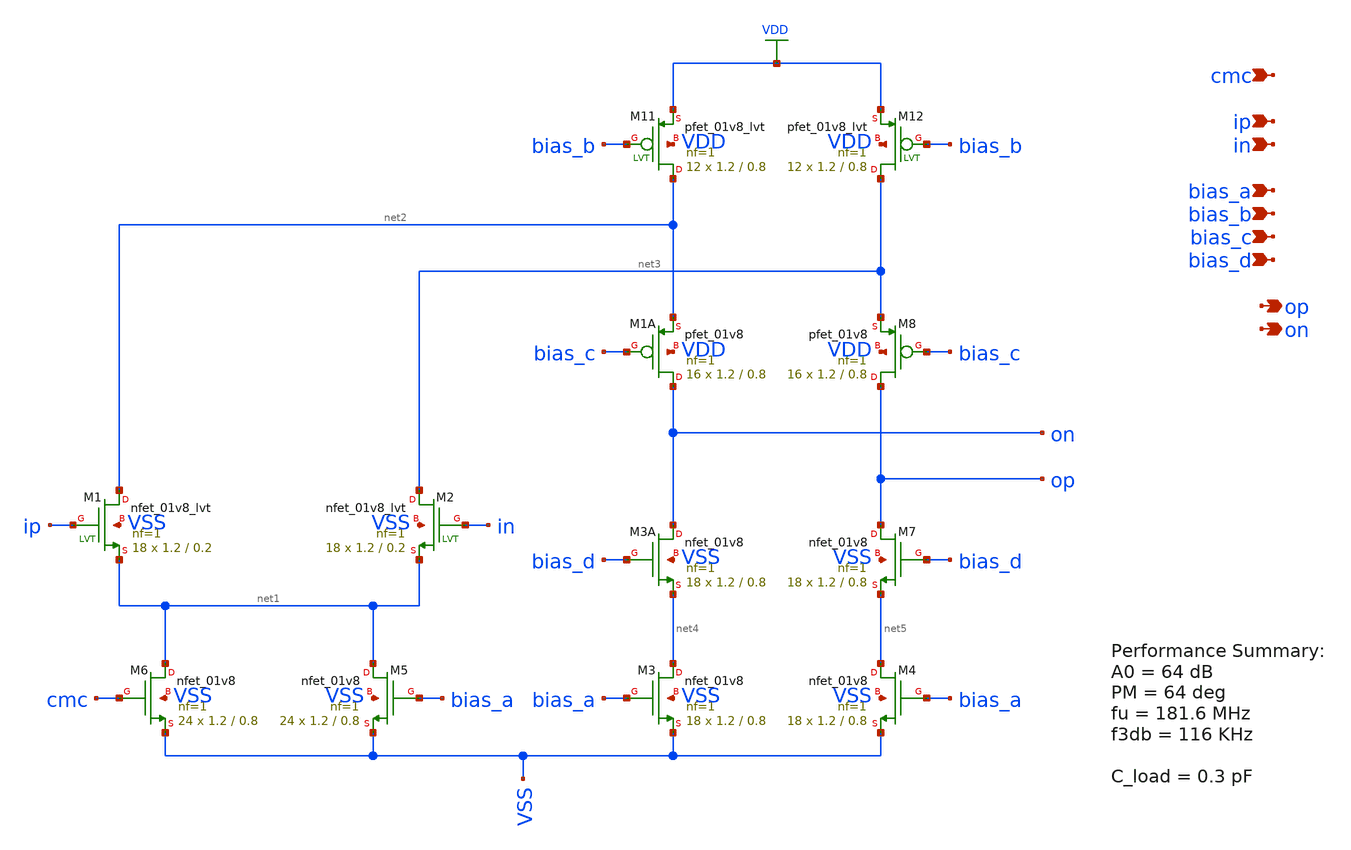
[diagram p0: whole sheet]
** sch_path: design/schematic/folded_cascode_2_core.sch
**.subckt folded_cascode_2_core cmc ip in bias_a bias_b bias_c bias_d op on
*.ipin cmc
*.ipin ip
*.ipin in
*.ipin bias_a
*.ipin bias_b
*.ipin bias_c
*.ipin bias_d
*.opin op
*.opin on
XM1 net2 ip net1 VSS sky130_fd_pr__nfet_01v8_lvt L=0.2 W=1.2 nf=1 ad='int((nf+1)/2) * W/nf * 0.29' as='int((nf+2)/2) * W/nf * 0.29'
+ pd='2*int((nf+1)/2) * (W/nf + 0.29)' ps='2*int((nf+2)/2) * (W/nf + 0.29)' nrd='0.29 / W' nrs='0.29 / W'
+ sa=0 sb=0 sd=0 mult=18 m=18
XM2 net3 in net1 VSS sky130_fd_pr__nfet_01v8_lvt L=0.2 W=1.2 nf=1 ad='int((nf+1)/2) * W/nf * 0.29' as='int((nf+2)/2) * W/nf * 0.29'
+ pd='2*int((nf+1)/2) * (W/nf + 0.29)' ps='2*int((nf+2)/2) * (W/nf + 0.29)' nrd='0.29 / W' nrs='0.29 / W'
+ sa=0 sb=0 sd=0 mult=18 m=18
XM6 net1 cmc VSS VSS sky130_fd_pr__nfet_01v8 L=0.8 W=1.2 nf=1 ad='int((nf+1)/2) * W/nf * 0.29' as='int((nf+2)/2) * W/nf * 0.29'
+ pd='2*int((nf+1)/2) * (W/nf + 0.29)' ps='2*int((nf+2)/2) * (W/nf + 0.29)' nrd='0.29 / W' nrs='0.29 / W'
+ sa=0 sb=0 sd=0 mult=24 m=24
XM5 net1 bias_a VSS VSS sky130_fd_pr__nfet_01v8 L=0.8 W=1.2 nf=1 ad='int((nf+1)/2) * W/nf * 0.29' as='int((nf+2)/2) * W/nf * 0.29'
+ pd='2*int((nf+1)/2) * (W/nf + 0.29)' ps='2*int((nf+2)/2) * (W/nf + 0.29)' nrd='0.29 / W' nrs='0.29 / W'
+ sa=0 sb=0 sd=0 mult=24 m=24
XM11 net2 bias_b VDD VDD sky130_fd_pr__pfet_01v8_lvt L=0.8 W=1.2 nf=1 ad='int((nf+1)/2) * W/nf * 0.29'
+ as='int((nf+2)/2) * W/nf * 0.29' pd='2*int((nf+1)/2) * (W/nf + 0.29)' ps='2*int((nf+2)/2) * (W/nf + 0.29)'
+ nrd='0.29 / W' nrs='0.29 / W' sa=0 sb=0 sd=0 mult=12 m=12
XM12 net3 bias_b VDD VDD sky130_fd_pr__pfet_01v8_lvt L=0.8 W=1.2 nf=1 ad='int((nf+1)/2) * W/nf * 0.29'
+ as='int((nf+2)/2) * W/nf * 0.29' pd='2*int((nf+1)/2) * (W/nf + 0.29)' ps='2*int((nf+2)/2) * (W/nf + 0.29)'
+ nrd='0.29 / W' nrs='0.29 / W' sa=0 sb=0 sd=0 mult=12 m=12
XM1A on bias_c net2 VDD sky130_fd_pr__pfet_01v8 L=0.8 W=1.2 nf=1 ad='int((nf+1)/2) * W/nf * 0.29' as='int((nf+2)/2) * W/nf * 0.29'
+ pd='2*int((nf+1)/2) * (W/nf + 0.29)' ps='2*int((nf+2)/2) * (W/nf + 0.29)' nrd='0.29 / W' nrs='0.29 / W'
+ sa=0 sb=0 sd=0 mult=16 m=16
XM8 op bias_c net3 VDD sky130_fd_pr__pfet_01v8 L=0.8 W=1.2 nf=1 ad='int((nf+1)/2) * W/nf * 0.29' as='int((nf+2)/2) * W/nf * 0.29'
+ pd='2*int((nf+1)/2) * (W/nf + 0.29)' ps='2*int((nf+2)/2) * (W/nf + 0.29)' nrd='0.29 / W' nrs='0.29 / W'
+ sa=0 sb=0 sd=0 mult=16 m=16
XM3A on bias_d net4 VSS sky130_fd_pr__nfet_01v8 L=0.8 W=1.2 nf=1 ad='int((nf+1)/2) * W/nf * 0.29' as='int((nf+2)/2) * W/nf * 0.29'
+ pd='2*int((nf+1)/2) * (W/nf + 0.29)' ps='2*int((nf+2)/2) * (W/nf + 0.29)' nrd='0.29 / W' nrs='0.29 / W'
+ sa=0 sb=0 sd=0 mult=18 m=18
XM7 op bias_d net5 VSS sky130_fd_pr__nfet_01v8 L=0.8 W=1.2 nf=1 ad='int((nf+1)/2) * W/nf * 0.29' as='int((nf+2)/2) * W/nf * 0.29'
+ pd='2*int((nf+1)/2) * (W/nf + 0.29)' ps='2*int((nf+2)/2) * (W/nf + 0.29)' nrd='0.29 / W' nrs='0.29 / W'
+ sa=0 sb=0 sd=0 mult=18 m=18
XM3 net4 bias_a VSS VSS sky130_fd_pr__nfet_01v8 L=0.8 W=1.2 nf=1 ad='int((nf+1)/2) * W/nf * 0.29' as='int((nf+2)/2) * W/nf * 0.29'
+ pd='2*int((nf+1)/2) * (W/nf + 0.29)' ps='2*int((nf+2)/2) * (W/nf + 0.29)' nrd='0.29 / W' nrs='0.29 / W'
+ sa=0 sb=0 sd=0 mult=18 m=18
XM4 net5 bias_a VSS VSS sky130_fd_pr__nfet_01v8 L=0.8 W=1.2 nf=1 ad='int((nf+1)/2) * W/nf * 0.29' as='int((nf+2)/2) * W/nf * 0.29'
+ pd='2*int((nf+1)/2) * (W/nf + 0.29)' ps='2*int((nf+2)/2) * (W/nf + 0.29)' nrd='0.29 / W' nrs='0.29 / W'
+ sa=0 sb=0 sd=0 mult=18 m=18
**.ends
.GLOBAL VDD
.end
